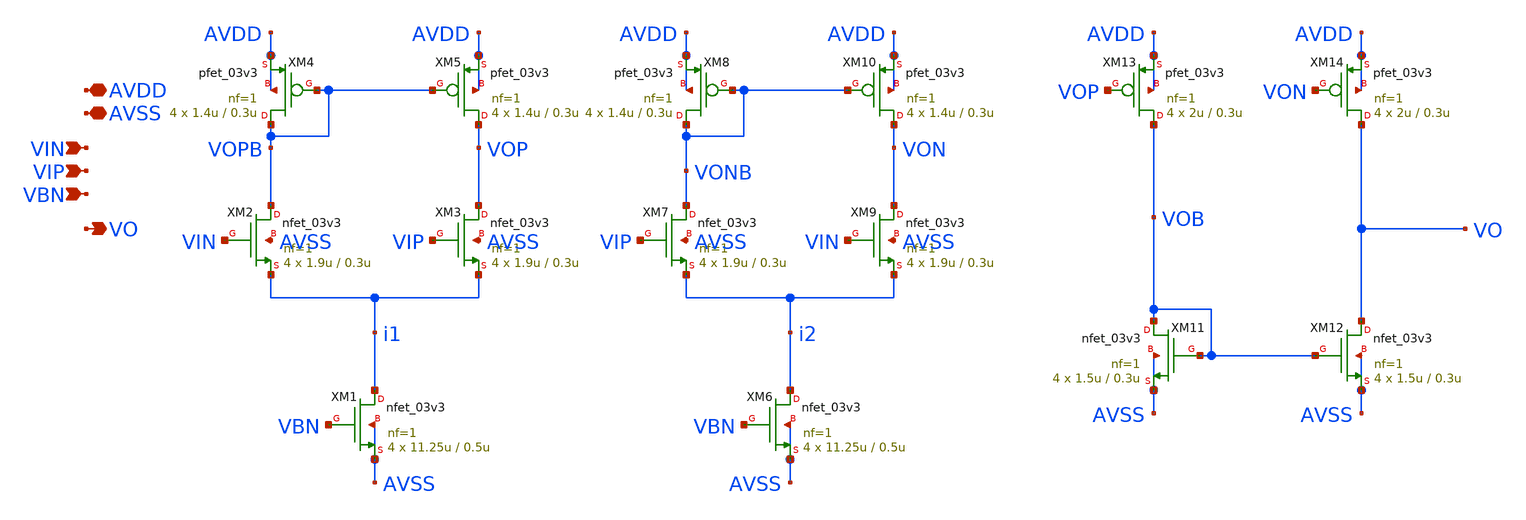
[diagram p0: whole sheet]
** sch_path: designs/libs/core_analog/d2s_converter/d2s_converter.sch
**.subckt d2s_converter AVDD AVSS VIN VIP VO VBN
*.iopin AVDD
*.iopin AVSS
*.ipin VIN
*.ipin VIP
*.opin VO
*.ipin VBN
XM2 VOPB VIN i1 AVSS nfet_03v3 L=0.3u W=1.9u nf=1 ad='int((nf+1)/2) * W/nf * 0.18u' as='int((nf+2)/2) * W/nf * 0.18u'
+ pd='2*int((nf+1)/2) * (W/nf + 0.18u)' ps='2*int((nf+2)/2) * (W/nf + 0.18u)' nrd='0.18u / W' nrs='0.18u / W'
+ sa=0 sb=0 sd=0 m=4
XM4 VOPB VOPB AVDD AVDD pfet_03v3 L=0.3u W=1.4u nf=1 ad='int((nf+1)/2) * W/nf * 0.18u' as='int((nf+2)/2) * W/nf * 0.18u'
+ pd='2*int((nf+1)/2) * (W/nf + 0.18u)' ps='2*int((nf+2)/2) * (W/nf + 0.18u)' nrd='0.18u / W' nrs='0.18u / W'
+ sa=0 sb=0 sd=0 m=4
XM11 VOB VOB AVSS AVSS nfet_03v3 L=0.3u W=1.5u nf=1 ad='int((nf+1)/2) * W/nf * 0.18u' as='int((nf+2)/2) * W/nf * 0.18u'
+ pd='2*int((nf+1)/2) * (W/nf + 0.18u)' ps='2*int((nf+2)/2) * (W/nf + 0.18u)' nrd='0.18u / W' nrs='0.18u / W'
+ sa=0 sb=0 sd=0 m=4
XM13 VOB VOP AVDD AVDD pfet_03v3 L=0.3u W=2u nf=1 ad='int((nf+1)/2) * W/nf * 0.18u' as='int((nf+2)/2) * W/nf * 0.18u'
+ pd='2*int((nf+1)/2) * (W/nf + 0.18u)' ps='2*int((nf+2)/2) * (W/nf + 0.18u)' nrd='0.18u / W' nrs='0.18u / W'
+ sa=0 sb=0 sd=0 m=4
XM3 VOP VIP i1 AVSS nfet_03v3 L=0.3u W=1.9u nf=1 ad='int((nf+1)/2) * W/nf * 0.18u' as='int((nf+2)/2) * W/nf * 0.18u'
+ pd='2*int((nf+1)/2) * (W/nf + 0.18u)' ps='2*int((nf+2)/2) * (W/nf + 0.18u)' nrd='0.18u / W' nrs='0.18u / W'
+ sa=0 sb=0 sd=0 m=4
XM5 VOP VOPB AVDD AVDD pfet_03v3 L=0.3u W=1.4u nf=1 ad='int((nf+1)/2) * W/nf * 0.18u' as='int((nf+2)/2) * W/nf * 0.18u'
+ pd='2*int((nf+1)/2) * (W/nf + 0.18u)' ps='2*int((nf+2)/2) * (W/nf + 0.18u)' nrd='0.18u / W' nrs='0.18u / W'
+ sa=0 sb=0 sd=0 m=4
XM7 VONB VIP i2 AVSS nfet_03v3 L=0.3u W=1.9u nf=1 ad='int((nf+1)/2) * W/nf * 0.18u' as='int((nf+2)/2) * W/nf * 0.18u'
+ pd='2*int((nf+1)/2) * (W/nf + 0.18u)' ps='2*int((nf+2)/2) * (W/nf + 0.18u)' nrd='0.18u / W' nrs='0.18u / W'
+ sa=0 sb=0 sd=0 m=4
XM8 VONB VONB AVDD AVDD pfet_03v3 L=0.3u W=1.4u nf=1 ad='int((nf+1)/2) * W/nf * 0.18u' as='int((nf+2)/2) * W/nf * 0.18u'
+ pd='2*int((nf+1)/2) * (W/nf + 0.18u)' ps='2*int((nf+2)/2) * (W/nf + 0.18u)' nrd='0.18u / W' nrs='0.18u / W'
+ sa=0 sb=0 sd=0 m=4
XM9 VON VIN i2 AVSS nfet_03v3 L=0.3u W=1.9u nf=1 ad='int((nf+1)/2) * W/nf * 0.18u' as='int((nf+2)/2) * W/nf * 0.18u'
+ pd='2*int((nf+1)/2) * (W/nf + 0.18u)' ps='2*int((nf+2)/2) * (W/nf + 0.18u)' nrd='0.18u / W' nrs='0.18u / W'
+ sa=0 sb=0 sd=0 m=4
XM10 VON VONB AVDD AVDD pfet_03v3 L=0.3u W=1.4u nf=1 ad='int((nf+1)/2) * W/nf * 0.18u' as='int((nf+2)/2) * W/nf * 0.18u'
+ pd='2*int((nf+1)/2) * (W/nf + 0.18u)' ps='2*int((nf+2)/2) * (W/nf + 0.18u)' nrd='0.18u / W' nrs='0.18u / W'
+ sa=0 sb=0 sd=0 m=4
XM14 VO VON AVDD AVDD pfet_03v3 L=0.3u W=2u nf=1 ad='int((nf+1)/2) * W/nf * 0.18u' as='int((nf+2)/2) * W/nf * 0.18u'
+ pd='2*int((nf+1)/2) * (W/nf + 0.18u)' ps='2*int((nf+2)/2) * (W/nf + 0.18u)' nrd='0.18u / W' nrs='0.18u / W'
+ sa=0 sb=0 sd=0 m=4
XM12 VO VOB AVSS AVSS nfet_03v3 L=0.3u W=1.5u nf=1 ad='int((nf+1)/2) * W/nf * 0.18u' as='int((nf+2)/2) * W/nf * 0.18u'
+ pd='2*int((nf+1)/2) * (W/nf + 0.18u)' ps='2*int((nf+2)/2) * (W/nf + 0.18u)' nrd='0.18u / W' nrs='0.18u / W'
+ sa=0 sb=0 sd=0 m=4
XM1 i1 VBN AVSS AVSS nfet_03v3 L=0.5u W=11.25u nf=1 ad='int((nf+1)/2) * W/nf * 0.18u' as='int((nf+2)/2) * W/nf * 0.18u'
+ pd='2*int((nf+1)/2) * (W/nf + 0.18u)' ps='2*int((nf+2)/2) * (W/nf + 0.18u)' nrd='0.18u / W' nrs='0.18u / W'
+ sa=0 sb=0 sd=0 m=4
XM6 i2 VBN AVSS AVSS nfet_03v3 L=0.5u W=11.25u nf=1 ad='int((nf+1)/2) * W/nf * 0.18u' as='int((nf+2)/2) * W/nf * 0.18u'
+ pd='2*int((nf+1)/2) * (W/nf + 0.18u)' ps='2*int((nf+2)/2) * (W/nf + 0.18u)' nrd='0.18u / W' nrs='0.18u / W'
+ sa=0 sb=0 sd=0 m=4
**.ends
.end
